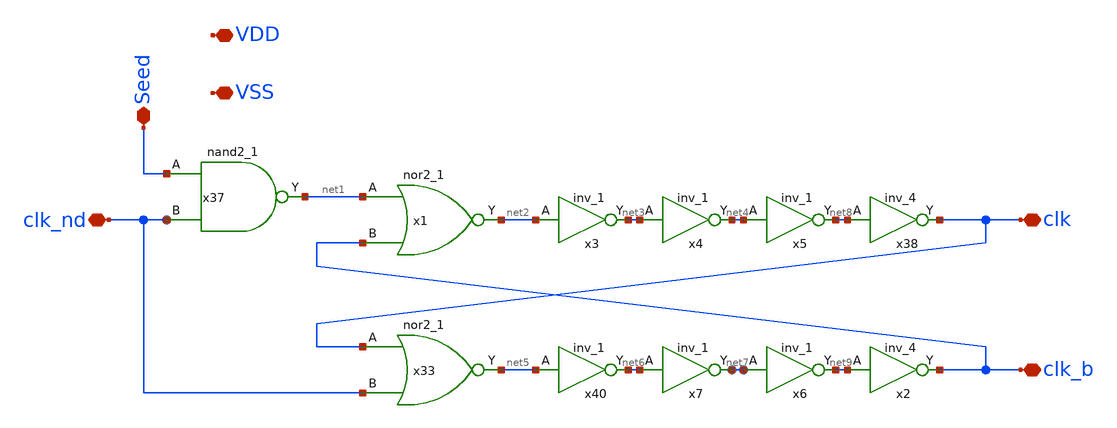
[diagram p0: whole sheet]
** sch_path: xschem/lib/Analog/NonOverlappingClk.sch
**.subckt NonOverlappingClk Seed VSS clk_nd clk clk_b VDD
*.iopin Seed
*.iopin VSS
*.iopin clk_nd
*.iopin clk
*.iopin clk_b
*.iopin VDD
x1 net1 clk_b VSS VSS VDD VDD net2 sky130_fd_sc_hd__nor2_1
x37 Seed clk_nd VSS VSS VDD VDD net1 sky130_fd_sc_hd__nand2_1
x33 clk clk_nd VSS VSS VDD VDD net5 sky130_fd_sc_hd__nor2_1
x38 net8 VSS VSS VDD VDD clk sky130_fd_sc_hd__inv_4
x40 net5 VSS VSS VDD VDD net6 sky130_fd_sc_hd__inv_1
x2 net9 VSS VSS VDD VDD clk_b sky130_fd_sc_hd__inv_4
x3 net2 VSS VSS VDD VDD net3 sky130_fd_sc_hd__inv_1
x4 net3 VSS VSS VDD VDD net4 sky130_fd_sc_hd__inv_1
x5 net4 VSS VSS VDD VDD net8 sky130_fd_sc_hd__inv_1
x6 net7 VSS VSS VDD VDD net9 sky130_fd_sc_hd__inv_1
x7 net6 VSS VSS VDD VDD net7 sky130_fd_sc_hd__inv_1
**.ends
.end
